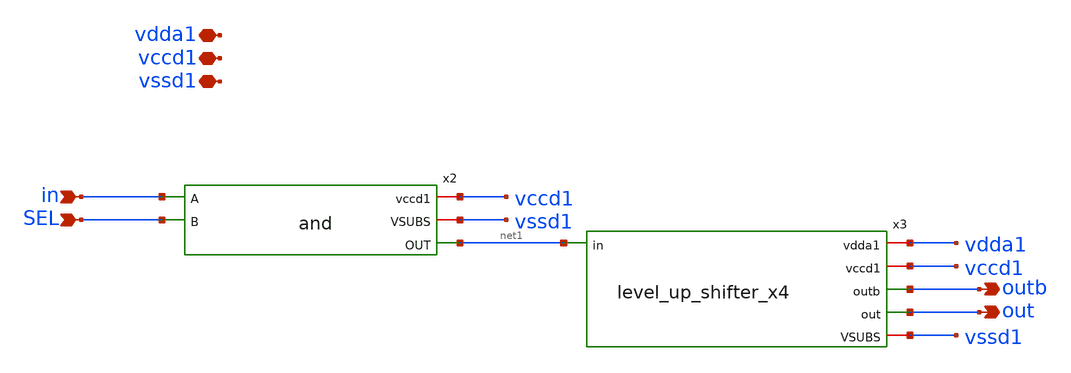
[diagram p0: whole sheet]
** sch_path: xschem/and_level_up_shifter_x4.sch
**.subckt and_level_up_shifter_x4 vccd1 vdda1 vssd1 in SEL out outb
*.iopin vccd1
*.iopin vdda1
*.iopin vssd1
*.ipin in
*.ipin SEL
*.opin out
*.opin outb
x2 vccd1 vssd1 in SEL net1 and
x3 vdda1 vccd1 net1 outb out vssd1 level_up_shifter_x4
**.ends
.end
